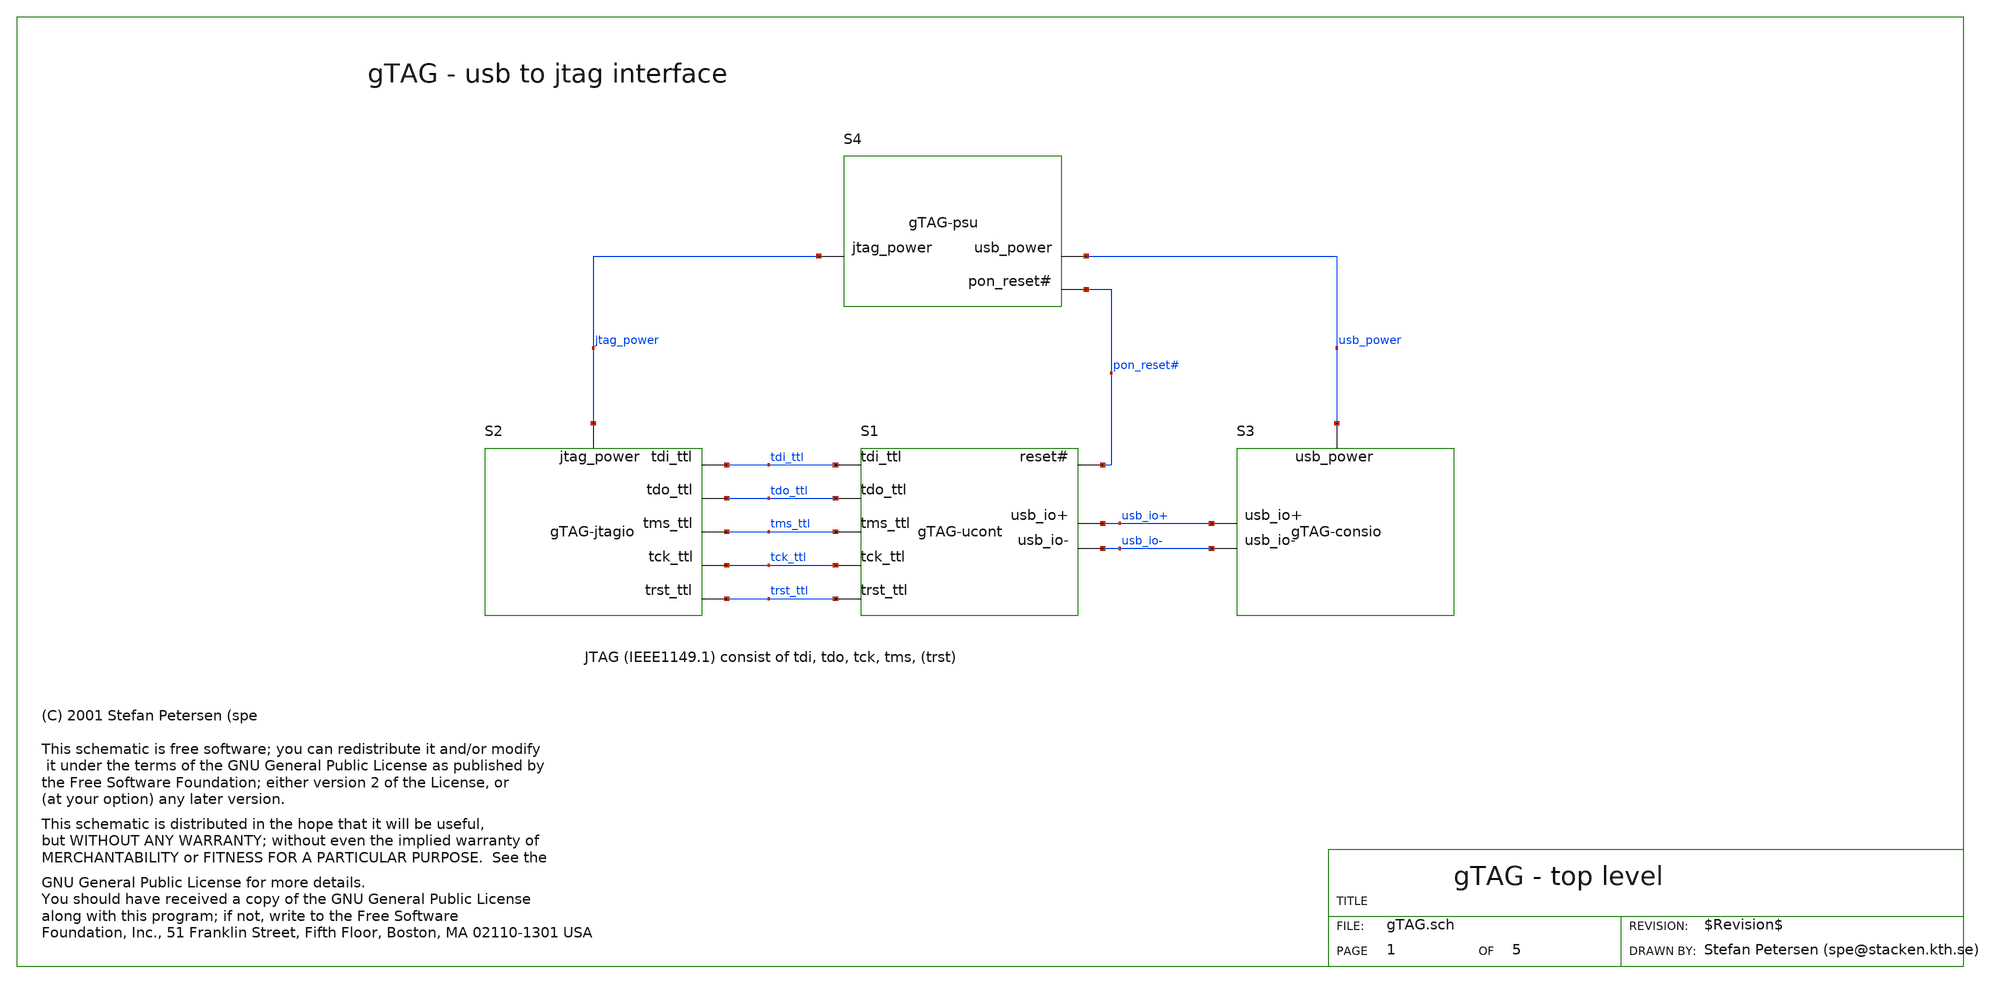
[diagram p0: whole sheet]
** sch_path: xschem-src/xschem_library/gschem_import/gTAG.sch
* Copyright (C) 1998-2026 Stefan Frederik Schippers
* This program is free software; you can redistribute it and/or modify
* it under the terms of the GNU General Public License as published by
* the Free Software Foundation; either version 2 of the License, or
* (at your option) any later version.
* This program is distributed in the hope that it will be useful,
* but WITHOUT ANY WARRANTY; without even the implied warranty of
* MERCHANTABILITY or FITNESS FOR A PARTICULAR PURPOSE.  See the
* GNU General Public License for more details.
* You should have received a copy of the GNU General Public License
* along with this program; if not, write to the Free Software
* copyleft.sym
**.subckt gTAG
S1 tdi_ttl tdo_ttl tms_ttl tck_ttl trst_ttl usb_io+ usb_io- pon_reset#
S2 tdi_ttl tdo_ttl tms_ttl tck_ttl trst_ttl jtag_power
S3 usb_io+ usb_io- usb_power
S4 jtag_power usb_power pon_reset#
S4
**.ends
.end
